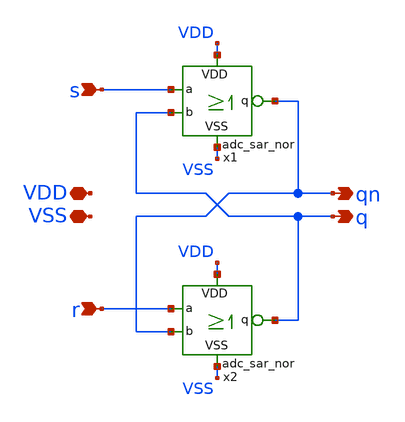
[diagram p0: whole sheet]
** sch_path: adc_sar_nor_latch.sch
**.subckt adc_sar_nor_latch VDD VSS s r q qn
*.iopin VDD
*.iopin VSS
*.ipin s
*.ipin r
*.opin q
*.opin qn
x1 q s VDD qn VSS adc_sar_nor
x2 qn r VDD q VSS adc_sar_nor
**.ends

* expanding   symbol:  adc_sar_nor.sym # of pins=5
** sym_path: adc_sar_nor.sym
** sch_path: adc_sar_nor.sch
.subckt adc_sar_nor b a VDD q VSS
*.iopin VDD
*.iopin VSS
*.ipin b
*.ipin a
*.opin q
XM1 q b VSS VSS nfet_03v3 L=0.28u W=0.42u nf=1 ad='int((nf+1)/2) * W/nf * 0.18u' as='int((nf+2)/2) * W/nf * 0.18u'
+ pd='2*int((nf+1)/2) * (W/nf + 0.18u)' ps='2*int((nf+2)/2) * (W/nf + 0.18u)' nrd='0.18u / W' nrs='0.18u / W'
+ sa=0 sb=0 sd=0 m=1
XM2 q a VSS VSS nfet_03v3 L=0.28u W=0.42u nf=1 ad='int((nf+1)/2) * W/nf * 0.18u' as='int((nf+2)/2) * W/nf * 0.18u'
+ pd='2*int((nf+1)/2) * (W/nf + 0.18u)' ps='2*int((nf+2)/2) * (W/nf + 0.18u)' nrd='0.18u / W' nrs='0.18u / W'
+ sa=0 sb=0 sd=0 m=1
XM5 net2 b VDD VDD pfet_03v3 L=0.28u W=0.8u nf=1 ad='int((nf+1)/2) * W/nf * 0.18u' as='int((nf+2)/2) * W/nf * 0.18u'
+ pd='2*int((nf+1)/2) * (W/nf + 0.18u)' ps='2*int((nf+2)/2) * (W/nf + 0.18u)' nrd='0.18u / W' nrs='0.18u / W'
+ sa=0 sb=0 sd=0 m=1
XM3 q a net2 VDD pfet_03v3 L=0.28u W=0.8u nf=1 ad='int((nf+1)/2) * W/nf * 0.18u' as='int((nf+2)/2) * W/nf * 0.18u'
+ pd='2*int((nf+1)/2) * (W/nf + 0.18u)' ps='2*int((nf+2)/2) * (W/nf + 0.18u)' nrd='0.18u / W' nrs='0.18u / W'
+ sa=0 sb=0 sd=0 m=1
XM4 q b net1 VDD pfet_03v3 L=0.28u W=0.8u nf=1 ad='int((nf+1)/2) * W/nf * 0.18u' as='int((nf+2)/2) * W/nf * 0.18u'
+ pd='2*int((nf+1)/2) * (W/nf + 0.18u)' ps='2*int((nf+2)/2) * (W/nf + 0.18u)' nrd='0.18u / W' nrs='0.18u / W'
+ sa=0 sb=0 sd=0 m=1
XM6 net1 a VDD VDD pfet_03v3 L=0.28u W=0.8u nf=1 ad='int((nf+1)/2) * W/nf * 0.18u' as='int((nf+2)/2) * W/nf * 0.18u'
+ pd='2*int((nf+1)/2) * (W/nf + 0.18u)' ps='2*int((nf+2)/2) * (W/nf + 0.18u)' nrd='0.18u / W' nrs='0.18u / W'
+ sa=0 sb=0 sd=0 m=1
.ends

.end
